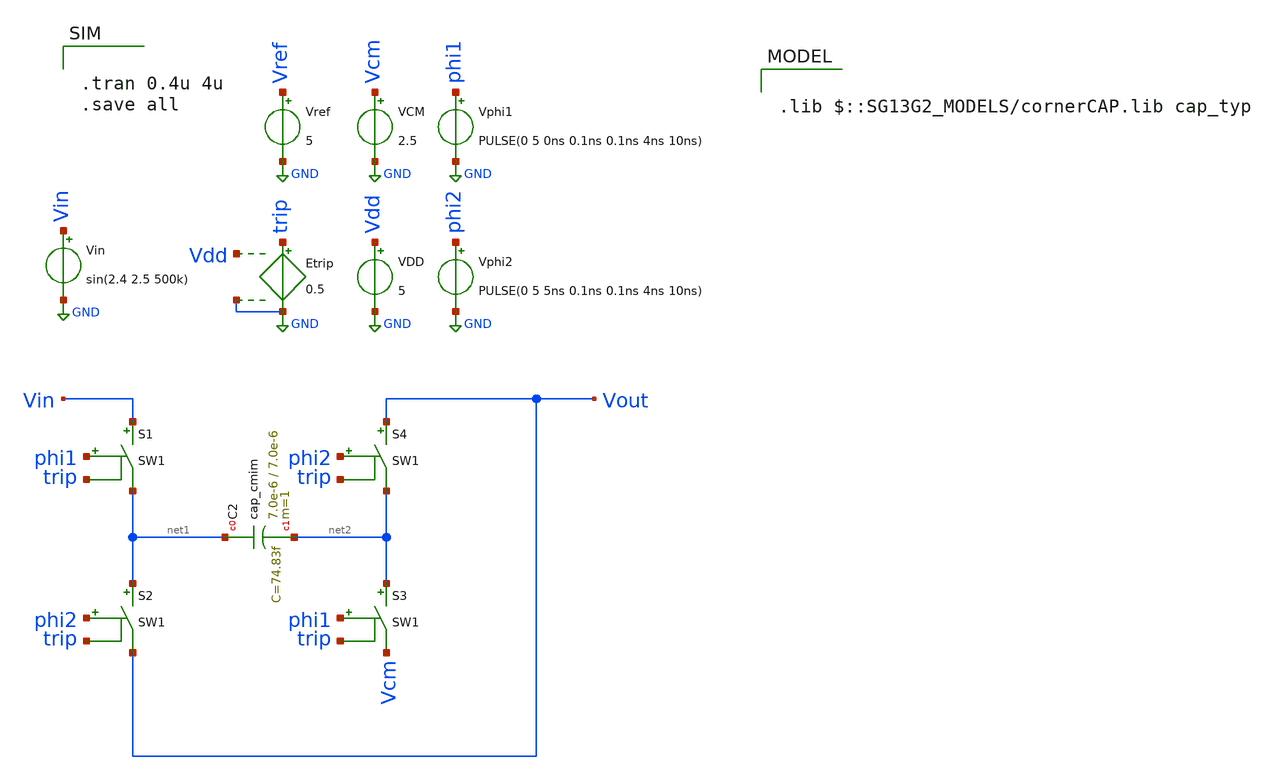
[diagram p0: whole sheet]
** sch_path: real_circuit/ideal_circuit_switches.sch
**.subckt ideal_circuit_switches
Etrip trip GND Vdd GND 0.5
Vref Vref GND 5
VDD Vdd GND 5
VCM Vcm GND 2.5
Vin Vin GND sin(2.4 2.5 500k)
Vphi1 phi1 GND PULSE(0 5 0ns 0.1ns 0.1ns 4ns 10ns)
Vphi2 phi2 GND PULSE(0 5 5ns 0.1ns 0.1ns 4ns 10ns)
S2 net1 Vout phi2 trip SW1
S1 Vin net1 phi1 trip SW1
S3 net2 Vcm phi1 trip SW1
S4 Vout net2 phi2 trip SW1
XC2 net1 net2 cap_cmim w=7.0e-6 l=7.0e-6 m=1 mm_ok=1
**** begin user architecture code


.tran 0.4u 4u
.save all



.lib $::SG13G2_MODELS/cornerCAP.lib cap_typ

**** end user architecture code
**.ends
.GLOBAL GND
**** begin user architecture code
.MODEL SW1 SW   VT=0.9 VH=0.01  RON=0.1 ROFF=10G
**** end user architecture code
.end
